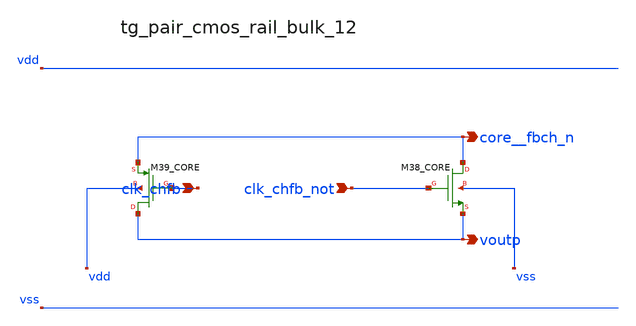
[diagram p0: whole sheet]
** sch_path: analog-db/raw/ia_006_fan_chopper_cmfb/hier/blocks/tg_pair_cmos_rail_bulk_12.sch
**.subckt tg_pair_cmos_rail_bulk_12 clk_chfb clk_chfb_not core__fbch_n voutp
*.ipin clk_chfb
*.ipin clk_chfb_not
*.opin core__fbch_n
*.opin voutp
XM38_CORE core__fbch_n clk_chfb_not voutp vss sg13_lv_nmos w=x_dut_xm38_core_w l=x_dut_xm38_core_l
+ ng=1 m=x_dut_xm38_core_m
XM39_CORE voutp clk_chfb core__fbch_n vdd sg13_lv_pmos w=x_dut_xm39_core_w l=x_dut_xm39_core_l ng=1
+ m=x_dut_xm39_core_m
**.ends
.end
